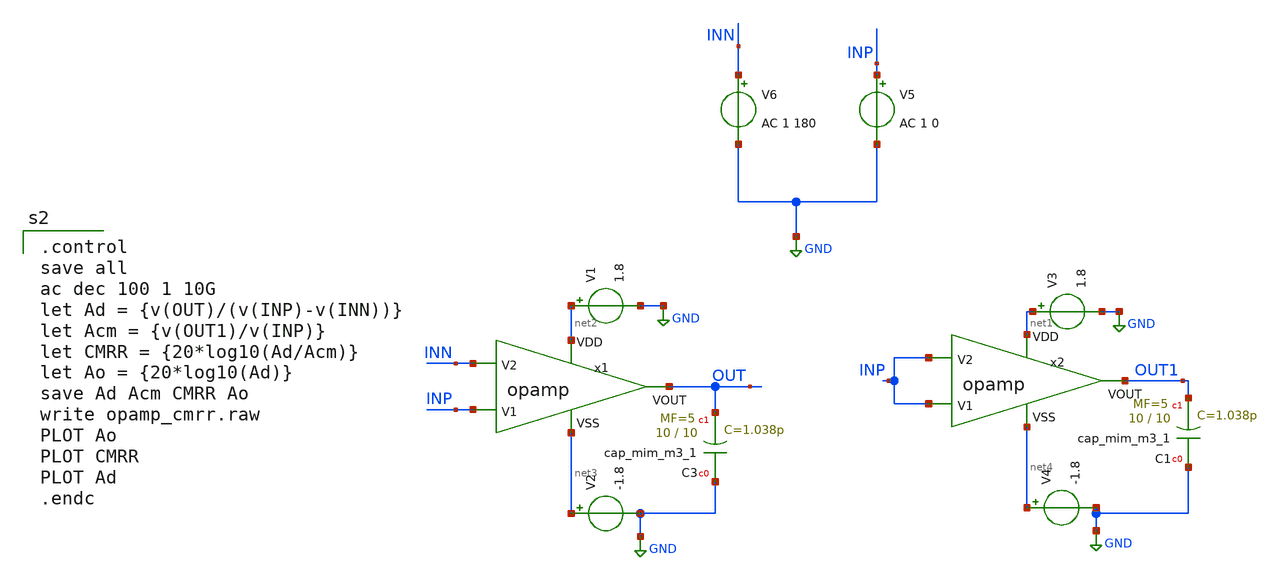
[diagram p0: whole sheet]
** sch_path: opamp_cmrr.sch
**.subckt opamp_cmrr
V6 INN GND AC 1 180
V5 INP GND AC 1 0
V1 net2 GND 1.8
V2 net3 GND -1.8
V3 net1 GND 1.8
V4 net4 GND -1.8
XC3 GND OUT sky130_fd_pr__cap_mim_m3_1 W=10 L=10 MF=5 m=5
XC1 GND net5 sky130_fd_pr__cap_mim_m3_1 W=10 L=10 MF=5 m=5
x1 net2 INN INP OUT net3 opamp
x2 net1 INP INP OUT1 net4 opamp
**** begin user architecture code

.control
save all
ac dec 100 1 10G
let Ad = {v(OUT)/(v(INP)-v(INN))}
let Acm = {v(OUT1)/v(INP)}
let CMRR = {20*log10(Ad/Acm)}
let Ao = {20*log10(Ad)}
save Ad Acm CMRR Ao
write opamp_cmrr.raw
PLOT Ao
PLOT CMRR
PLOT Ad
.endc


** opencircuitdesign pdks install
.lib $::SKYWATER_MODELS/sky130.lib.spice tt


**** end user architecture code
**.ends

* expanding   symbol:  /foss/designs/FINAL_PROJECT_KTMDT/opamp.sym # of pins=5
** sym_path: /foss/designs/FINAL_PROJECT_KTMDT/opamp.sym
** sch_path: /foss/designs/FINAL_PROJECT_KTMDT/opamp.sch
.subckt opamp VDD V2 V1 VOUT VSS
*.ipin VSS
*.ipin VDD
*.ipin V2
*.ipin V1
*.opin VOUT
XM3 net4 V2 net1 VSS sky130_fd_pr__nfet_g5v0d10v5 L=1 W=17.45 nf=1 ad='int((nf+1)/2) * W/nf * 0.29' as='int((nf+2)/2) * W/nf * 0.29'
+ pd='2*int((nf+1)/2) * (W/nf + 0.29)' ps='2*int((nf+2)/2) * (W/nf + 0.29)' nrd='0.29 / W' nrs='0.29 / W'
+ sa=0 sb=0 sd=0 mult=1 m=1
XM1 net5 net4 VDD VDD sky130_fd_pr__pfet_g5v0d10v5 L=1 W=30 nf=1 ad='int((nf+1)/2) * W/nf * 0.29' as='int((nf+2)/2) * W/nf * 0.29'
+ pd='2*int((nf+1)/2) * (W/nf + 0.29)' ps='2*int((nf+2)/2) * (W/nf + 0.29)' nrd='0.29 / W' nrs='0.29 / W'
+ sa=0 sb=0 sd=0 mult=1 m=1
XM4 net5 V1 net1 VSS sky130_fd_pr__nfet_g5v0d10v5 L=1 W=17.45 nf=1 ad='int((nf+1)/2) * W/nf * 0.29' as='int((nf+2)/2) * W/nf * 0.29'
+ pd='2*int((nf+1)/2) * (W/nf + 0.29)' ps='2*int((nf+2)/2) * (W/nf + 0.29)' nrd='0.29 / W' nrs='0.29 / W'
+ sa=0 sb=0 sd=0 mult=1 m=1
XM6 net1 net6 VSS VSS sky130_fd_pr__nfet_g5v0d10v5 L=1 W=15.17 nf=1 ad='int((nf+1)/2) * W/nf * 0.29'
+ as='int((nf+2)/2) * W/nf * 0.29' pd='2*int((nf+1)/2) * (W/nf + 0.29)' ps='2*int((nf+2)/2) * (W/nf + 0.29)'
+ nrd='0.29 / W' nrs='0.29 / W' sa=0 sb=0 sd=0 mult=1 m=1
XM7 VOUT net6 VSS VSS sky130_fd_pr__nfet_g5v0d10v5 L=1 W=19 nf=1 ad='int((nf+1)/2) * W/nf * 0.29' as='int((nf+2)/2) * W/nf * 0.29'
+ pd='2*int((nf+1)/2) * (W/nf + 0.29)' ps='2*int((nf+2)/2) * (W/nf + 0.29)' nrd='0.29 / W' nrs='0.29 / W'
+ sa=0 sb=0 sd=0 mult=1 m=1
XM5 net6 net6 VSS VSS sky130_fd_pr__nfet_g5v0d10v5 L=1 W=15.17 nf=1 ad='int((nf+1)/2) * W/nf * 0.29'
+ as='int((nf+2)/2) * W/nf * 0.29' pd='2*int((nf+1)/2) * (W/nf + 0.29)' ps='2*int((nf+2)/2) * (W/nf + 0.29)'
+ nrd='0.29 / W' nrs='0.29 / W' sa=0 sb=0 sd=0 mult=1 m=1
XM2 net4 net4 VDD VDD sky130_fd_pr__pfet_g5v0d10v5 L=1 W=30 nf=1 ad='int((nf+1)/2) * W/nf * 0.29' as='int((nf+2)/2) * W/nf * 0.29'
+ pd='2*int((nf+1)/2) * (W/nf + 0.29)' ps='2*int((nf+2)/2) * (W/nf + 0.29)' nrd='0.29 / W' nrs='0.29 / W'
+ sa=0 sb=0 sd=0 mult=1 m=1
XM8 VOUT net5 VDD VDD sky130_fd_pr__pfet_g5v0d10v5 L=1 W=38 nf=1 ad='int((nf+1)/2) * W/nf * 0.29' as='int((nf+2)/2) * W/nf * 0.29'
+ pd='2*int((nf+1)/2) * (W/nf + 0.29)' ps='2*int((nf+2)/2) * (W/nf + 0.29)' nrd='0.29 / W' nrs='0.29 / W'
+ sa=0 sb=0 sd=0 mult=2 m=2
V_ibias net7 net6 0
.save i(v_ibias)
XR1 net2 VDD VSS sky130_fd_pr__res_high_po W=1 L=41.1 mult=1 m=1
XR2 net3 net2 VSS sky130_fd_pr__res_high_po W=1 L=41.1 mult=1 m=1
XR3 net7 net3 VSS sky130_fd_pr__res_high_po W=1 L=41.1 mult=1 m=1
XR4 net8 VOUT VSS sky130_fd_pr__res_high_po W=1 L=5 mult=1 m=1
XC1 net8 net5 sky130_fd_pr__cap_mim_m3_1 W=9 L=9 MF=2 m=2
.ends

.GLOBAL GND
.end
